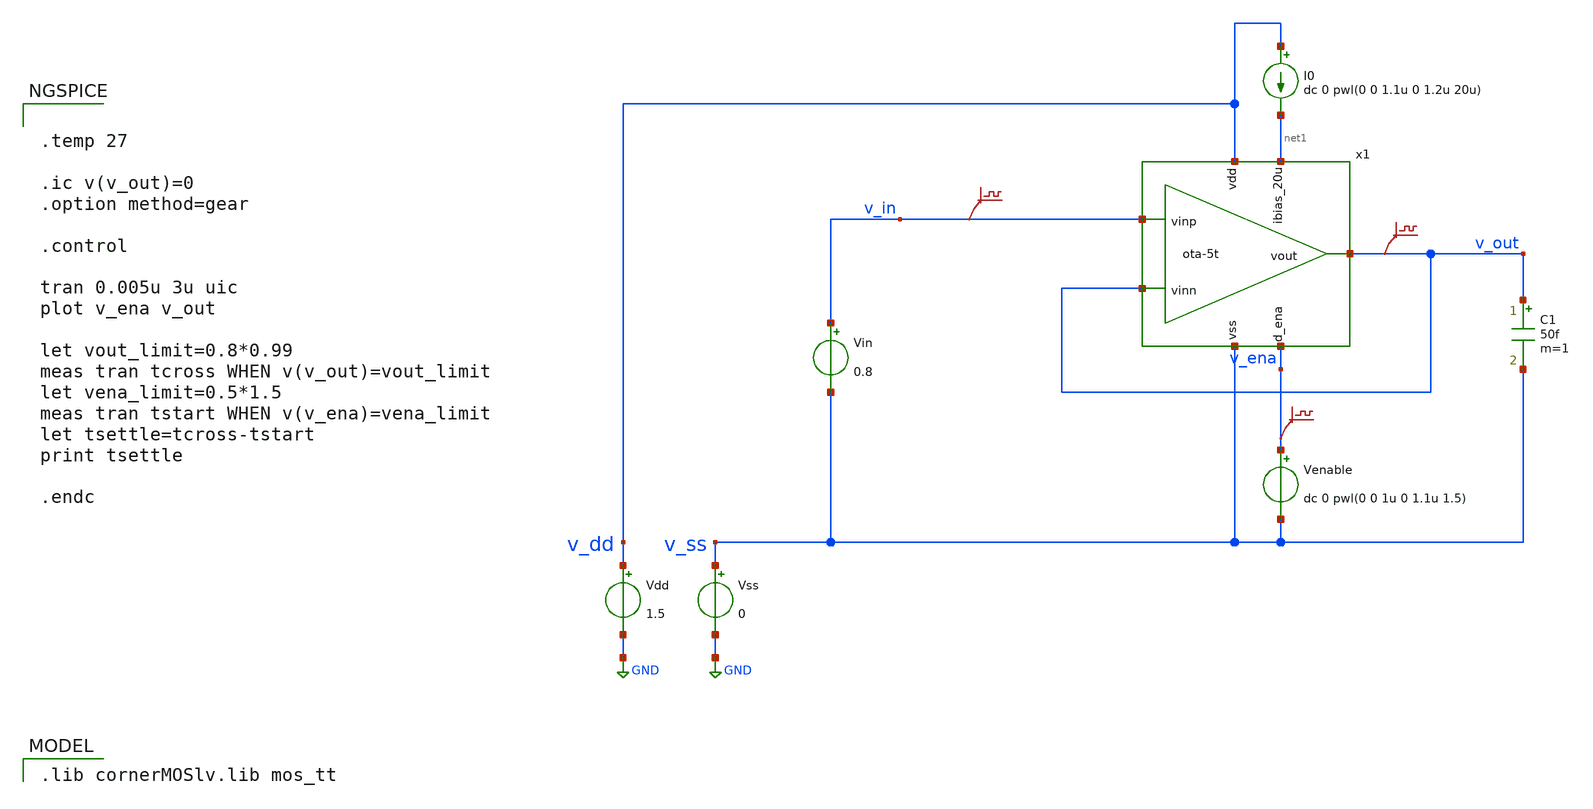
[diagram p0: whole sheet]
** sch_path: 004_Real_Circuits/001_version_basic_ota_pretl/ota-5t_tb-tran.sch
* (c) 2024-2025 Harald Pretl, Apache-2.0 license
**.subckt ota-5t_tb-tran
Vdd v_dd GND 1.5
Vss v_ss GND 0
C1 v_out v_ss 50f m=1
Vin v_in v_ss 0.8
I0 v_dd net1 dc 0 pwl(0 0 1.1u 0 1.2u 20u)
.save v(v_in)
.save v(v_out)
x1 v_dd v_out v_in v_out net1 v_ena v_ss ota-5t
Venable v_ena v_ss dc 0 pwl(0 0 1u 0 1.1u 1.5)
.save v(v_ena)
**** begin user architecture code
 .lib cornerMOSlv.lib mos_tt



.temp 27

.ic v(v_out)=0
.option method=gear

.control

tran 0.005u 3u uic
plot v_ena v_out

let vout_limit=0.8*0.99
meas tran tcross WHEN v(v_out)=vout_limit
let vena_limit=0.5*1.5
meas tran tstart WHEN v(v_ena)=vena_limit
let tsettle=tcross-tstart
print tsettle

.endc


**** end user architecture code
**.ends

* expanding   symbol:  004_Real_Circuits/001_version_basic_ota_pretl/ota-5t.sym # of pins=7
** sym_path: 004_Real_Circuits/001_version_basic_ota_pretl/ota-5t.sym
** sch_path: 004_Real_Circuits/001_version_basic_ota_pretl/ota-5t.sch
.subckt ota-5t vdd vout vinp vinn ibias_20u d_ena vss
*.ipin ibias_20u
*.iopin vdd
*.iopin vss
*.ipin vinp
*.ipin vinn
*.opin vout
*.ipin d_ena
XM5 tail gate_n vss vss sg13_lv_nmos w=1.5u l=5u ng=1 m=1 mm_ok=1
XM4 vout gate_p vdd vdd sg13_lv_pmos w=3.5u l=5u ng=1 m=1 mm_ok=1
XM1 gate_p vinp tail vss sg13_lv_nmos w=2u l=5u ng=1 m=1 mm_ok=1
XM2 vout vinn tail vss sg13_lv_nmos w=2u l=5u ng=1 m=1 mm_ok=1
XM3 gate_p gate_p vdd vdd sg13_lv_pmos w=3.5u l=5u ng=1 m=1 mm_ok=1
XM6 ibias_20u gate_n vss vss sg13_lv_nmos w=10u l=5u ng=5 m=1 mm_ok=1
XM9 gate_n ena_n vss vss sg13_lv_nmos w=0.5u l=0.13u ng=1 m=1 mm_ok=1
XM11 gate_p ena vdd vdd sg13_lv_pmos w=1.5u l=0.13u ng=1 m=1 mm_ok=1
XM7 ena ena_n vss vss sg13_lv_nmos w=0.5u l=0.13u ng=1 m=1 mm_ok=1
XM8 ena ena_n vdd vdd sg13_lv_pmos w=1.5u l=0.13u ng=1 m=1 mm_ok=1
XM10 ibias_20u ena gate_n vss sg13_lv_nmos w=0.5u l=0.13u ng=1 m=1 mm_ok=1
XM12 ena_n d_ena vss vss sg13_lv_nmos w=0.5u l=0.13u ng=1 m=1 mm_ok=1
XM13 ena_n d_ena vdd vdd sg13_lv_pmos w=1.5u l=0.13u ng=1 m=1 mm_ok=1
.ends

.GLOBAL GND
.end
